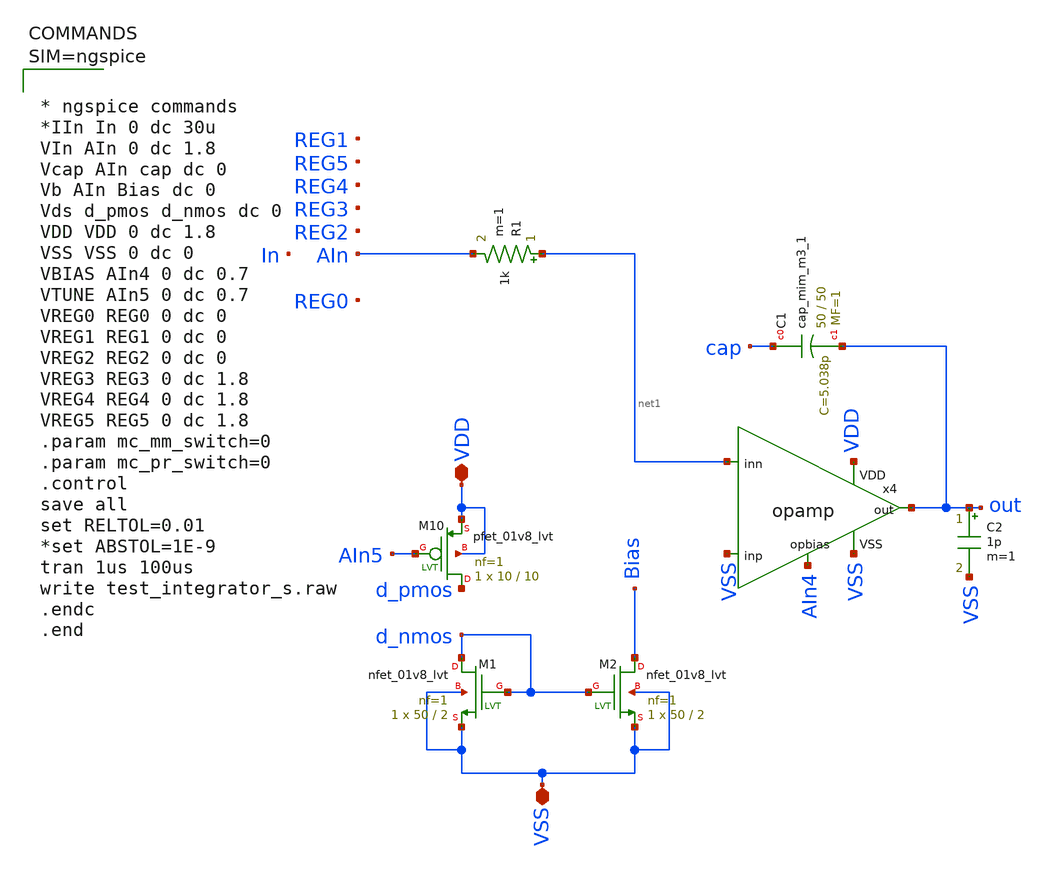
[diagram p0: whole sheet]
** sch_path: xschem/test_integrator_s.sch
**.subckt test_integrator_s VSS VDD
*.iopin VSS
*.iopin VDD
XM1 d_nmos d_nmos VSS VSS sky130_fd_pr__nfet_01v8_lvt L=2 W=50 nf=1 ad='int((1 + 1)/2) * 50 / 1 * 0.29'
+ as='int((1 + 2)/2) * 50 / 1 * 0.29' pd='2*int((1 + 1)/2) * (50 / 1 + 0.29)' ps='2*int((1 + 2)/2) * (50 / 1 + 0.29)'
+ nrd='0.29 / 50 ' nrs='0.29 / 50 ' sa=0 sb=0 sd=0 mult=1 m=1
XM2 Bias d_nmos VSS VSS sky130_fd_pr__nfet_01v8_lvt L=2 W=50 nf=1 ad='int((1 + 1)/2) * 50 / 1 * 0.29'
+ as='int((1 + 2)/2) * 50 / 1 * 0.29' pd='2*int((1 + 1)/2) * (50 / 1 + 0.29)' ps='2*int((1 + 2)/2) * (50 / 1 + 0.29)'
+ nrd='0.29 / 50 ' nrs='0.29 / 50 ' sa=0 sb=0 sd=0 mult=1 m=1
XM10 d_pmos AIn5 VDD VDD sky130_fd_pr__pfet_01v8_lvt L=10 W=10 nf=1 ad='int((1 + 1)/2) * 10 / 1 * 0.29'
+ as='int((1 + 2)/2) * 10 / 1 * 0.29' pd='2*int((1 + 1)/2) * (10 / 1 + 0.29)' ps='2*int((1 + 2)/2) * (10 / 1 + 0.29)'
+ nrd='0.29 / 10 ' nrs='0.29 / 10 ' sa=0 sb=0 sd=0 mult=1 m=1
XC1 cap out sky130_fd_pr__cap_mim_m3_1 W=50 L=50 MF=1 m=1
x4 AIn4 VSS net1 out VSS VDD opamp
C2 out VSS 1p m=1
R1 net1 AIn 1k m=1
**** begin user architecture code

** opencircuitdesign pdks install
.lib $::SKYWATER_MODELS/sky130.lib.spice tt





* ngspice commands
*IIn In 0 dc 30u
VIn AIn 0 dc 1.8
Vcap AIn cap dc 0
Vb AIn Bias dc 0
Vds d_pmos d_nmos dc 0
VDD VDD 0 dc 1.8
VSS VSS 0 dc 0
VBIAS AIn4 0 dc 0.7
VTUNE AIn5 0 dc 0.7
VREG0 REG0 0 dc 0
VREG1 REG1 0 dc 0
VREG2 REG2 0 dc 0
VREG3 REG3 0 dc 1.8
VREG4 REG4 0 dc 1.8
VREG5 REG5 0 dc 1.8
.param mc_mm_switch=0
.param mc_pr_switch=0
.control
save all
set RELTOL=0.01
*set ABSTOL=1E-9
tran 1us 100us
write test_integrator_s.raw
.endc
.end


**** end user architecture code
**.ends

* expanding   symbol:  opamp/opamp.sym # of pins=6
** sym_path: xschem/opamp/opamp.sym
** sch_path: xschem/opamp/opamp.sch
.subckt opamp opbias inp inn out VSS VDD
*.ipin inp
*.ipin inn
*.ipin opbias
*.opin out
*.iopin VDD
*.iopin VSS
XC1 net5 out sky130_fd_pr__cap_mim_m3_1 W=2 L=4 MF=1 m=1
XC2 out net4 sky130_fd_pr__cap_mim_m3_1 W=2 L=4 MF=1 m=1
XM26 net2 opbias VDD VDD sky130_fd_pr__pfet_01v8_lvt L=3 W=10 nf=4 ad='int((4 + 1)/2) * 10 / 4 * 0.29'
+ as='int((4 + 2)/2) * 10 / 4 * 0.29' pd='2*int((4 + 1)/2) * (10 / 4 + 0.29)' ps='2*int((4 + 2)/2) * (10 / 4 + 0.29)'
+ nrd='0.29 / 10 ' nrs='0.29 / 10 ' sa=0 sb=0 sd=0 mult=1 m=1
XM3 net1 net1 VDD VDD sky130_fd_pr__pfet_01v8_lvt L=3 W=10 nf=2 ad='int((2 + 1)/2) * 10 / 2 * 0.29' as='int((2 + 2)/2) * 10 / 2 * 0.29'
+ pd='2*int((2 + 1)/2) * (10 / 2 + 0.29)' ps='2*int((2 + 2)/2) * (10 / 2 + 0.29)' nrd='0.29 / 10 ' nrs='0.29 / 10 '
+ sa=0 sb=0 sd=0 mult=1 m=1
XM4 net5 net1 VDD VDD sky130_fd_pr__pfet_01v8_lvt L=3 W=10 nf=2 ad='int((2 + 1)/2) * 10 / 2 * 0.29' as='int((2 + 2)/2) * 10 / 2 * 0.29'
+ pd='2*int((2 + 1)/2) * (10 / 2 + 0.29)' ps='2*int((2 + 2)/2) * (10 / 2 + 0.29)' nrd='0.29 / 10 ' nrs='0.29 / 10 '
+ sa=0 sb=0 sd=0 mult=1 m=1
XM10 out net5 VDD VDD sky130_fd_pr__pfet_01v8_lvt L=3 W=100 nf=5 ad='int((5 + 1)/2) * 100 / 5 * 0.29'
+ as='int((5 + 2)/2) * 100 / 5 * 0.29' pd='2*int((5 + 1)/2) * (100 / 5 + 0.29)' ps='2*int((5 + 2)/2) * (100 / 5 + 0.29)'
+ nrd='0.29 / 100 ' nrs='0.29 / 100 ' sa=0 sb=0 sd=0 mult=1 m=1
XM17 out net4 VSS VSS sky130_fd_pr__nfet_01v8_lvt L=3 W=80 nf=5 ad='int((5 + 1)/2) * 80 / 5 * 0.29' as='int((5 + 2)/2) * 80 / 5 * 0.29'
+ pd='2*int((5 + 1)/2) * (80 / 5 + 0.29)' ps='2*int((5 + 2)/2) * (80 / 5 + 0.29)' nrd='0.29 / 80 ' nrs='0.29 / 80 '
+ sa=0 sb=0 sd=0 mult=1 m=1
XM19 net4 net3 VSS VSS sky130_fd_pr__nfet_01v8_lvt L=3 W=5 nf=1 ad='int((1 + 1)/2) * 5 / 1 * 0.29' as='int((1 + 2)/2) * 5 / 1 * 0.29'
+ pd='2*int((1 + 1)/2) * (5 / 1 + 0.29)' ps='2*int((1 + 2)/2) * (5 / 1 + 0.29)' nrd='0.29 / 5 ' nrs='0.29 / 5 '
+ sa=0 sb=0 sd=0 mult=1 m=1
XM20 net3 net3 VSS VSS sky130_fd_pr__nfet_01v8_lvt L=3 W=5 nf=1 ad='int((1 + 1)/2) * 5 / 1 * 0.29' as='int((1 + 2)/2) * 5 / 1 * 0.29'
+ pd='2*int((1 + 1)/2) * (5 / 1 + 0.29)' ps='2*int((1 + 2)/2) * (5 / 1 + 0.29)' nrd='0.29 / 5 ' nrs='0.29 / 5 '
+ sa=0 sb=0 sd=0 mult=1 m=1
XM2 net1 net4 VSS VSS sky130_fd_pr__nfet_01v8_lvt L=3 W=8 nf=1 ad='int((1 + 1)/2) * 8 / 1 * 0.29' as='int((1 + 2)/2) * 8 / 1 * 0.29'
+ pd='2*int((1 + 1)/2) * (8 / 1 + 0.29)' ps='2*int((1 + 2)/2) * (8 / 1 + 0.29)' nrd='0.29 / 8 ' nrs='0.29 / 8 '
+ sa=0 sb=0 sd=0 mult=1 m=1
XM5 net5 net3 VSS VSS sky130_fd_pr__nfet_01v8_lvt L=3 W=8 nf=1 ad='int((1 + 1)/2) * 8 / 1 * 0.29' as='int((1 + 2)/2) * 8 / 1 * 0.29'
+ pd='2*int((1 + 1)/2) * (8 / 1 + 0.29)' ps='2*int((1 + 2)/2) * (8 / 1 + 0.29)' nrd='0.29 / 8 ' nrs='0.29 / 8 '
+ sa=0 sb=0 sd=0 mult=1 m=1
XM1 net3 inn net2 VDD sky130_fd_pr__pfet_01v8_lvt L=3 W=15 nf=3 ad='int((3 + 1)/2) * 15 / 3 * 0.29' as='int((3 + 2)/2) * 15 / 3 * 0.29'
+ pd='2*int((3 + 1)/2) * (15 / 3 + 0.29)' ps='2*int((3 + 2)/2) * (15 / 3 + 0.29)' nrd='0.29 / 15 ' nrs='0.29 / 15 '
+ sa=0 sb=0 sd=0 mult=1 m=1
XM6 net4 inp net2 VDD sky130_fd_pr__pfet_01v8_lvt L=3 W=15 nf=3 ad='int((3 + 1)/2) * 15 / 3 * 0.29' as='int((3 + 2)/2) * 15 / 3 * 0.29'
+ pd='2*int((3 + 1)/2) * (15 / 3 + 0.29)' ps='2*int((3 + 2)/2) * (15 / 3 + 0.29)' nrd='0.29 / 15 ' nrs='0.29 / 15 '
+ sa=0 sb=0 sd=0 mult=1 m=1
.ends

.end
